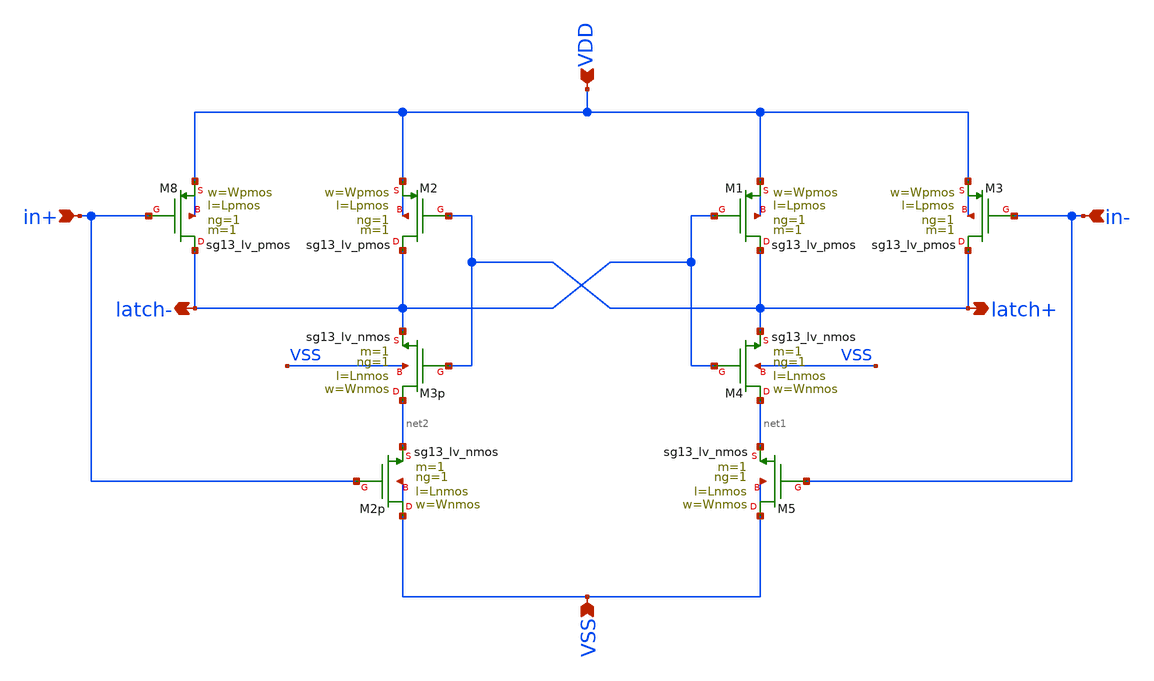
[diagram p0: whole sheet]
** sch_path: zip_meiners/ic_design/design_comp/latch_stage_test.sch
**.subckt latch_stage_test in+ in- VDD VSS latch+ latch-
*.ipin in+
*.ipin in-
*.ipin VDD
*.ipin VSS
*.opin latch+
*.opin latch-
XM8 latch- in+ VDD VDD sg13_lv_pmos w=Wpmos l=Lpmos ng=1 m=1 mm_ok=1
XM1 latch+ latch- VDD VDD sg13_lv_pmos w=Wpmos l=Lpmos ng=1 m=1 mm_ok=1
XM2 latch- latch+ VDD VDD sg13_lv_pmos w=Wpmos l=Lpmos ng=1 m=1 mm_ok=1
XM3 latch+ in- VDD VDD sg13_lv_pmos w=Wpmos l=Lpmos ng=1 m=1 mm_ok=1
XM3p net2 latch+ latch- VSS sg13_lv_nmos w=Wnmos l=Lnmos ng=1 m=1 mm_ok=1
XM2p VSS in+ net2 VSS sg13_lv_nmos w=Wnmos l=Lnmos ng=1 m=1 mm_ok=1
XM4 net1 latch- latch+ VSS sg13_lv_nmos w=Wnmos l=Lnmos ng=1 m=1 mm_ok=1
XM5 VSS in- net1 VSS sg13_lv_nmos w=Wnmos l=Lnmos ng=1 m=1 mm_ok=1
**.ends
.end
